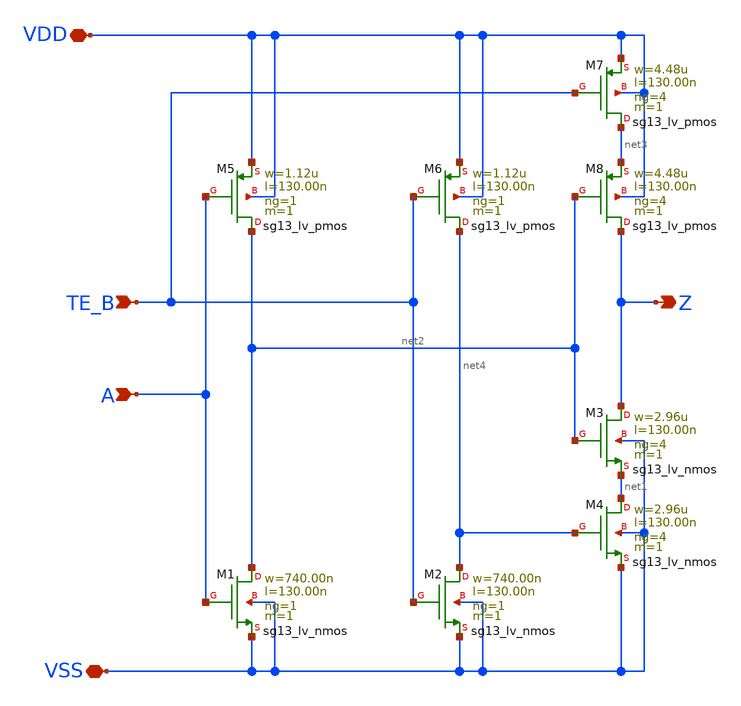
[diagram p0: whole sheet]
** sch_path: ihp-sg13g2/libs.tech/xschem/sg13g2_stdcells/sg13g2_ebufn_4.sch
**.subckt sg13g2_ebufn_4 A TE_B Z VDD VSS
*.ipin A
*.ipin TE_B
*.opin Z
*.iopin VDD
*.iopin VSS
XM1 net2 A VSS VSS sg13_lv_nmos w=740.00n l=130.00n ng=1 m=1 mm_ok=1
XM2 net4 TE_B VSS VSS sg13_lv_nmos w=740.00n l=130.00n ng=1 m=1 mm_ok=1
XM3 Z net2 net1 VSS sg13_lv_nmos w=2.96u l=130.00n ng=4 m=1 mm_ok=1
XM4 net1 net4 VSS VSS sg13_lv_nmos w=2.96u l=130.00n ng=4 m=1 mm_ok=1
XM5 net2 A VDD VDD sg13_lv_pmos w=1.12u l=130.00n ng=1 m=1 mm_ok=1
XM6 net4 TE_B VDD VDD sg13_lv_pmos w=1.12u l=130.00n ng=1 m=1 mm_ok=1
XM7 net3 TE_B VDD VDD sg13_lv_pmos w=4.48u l=130.00n ng=4 m=1 mm_ok=1
XM8 Z net2 net3 VDD sg13_lv_pmos w=4.48u l=130.00n ng=4 m=1 mm_ok=1
**.ends
.end
